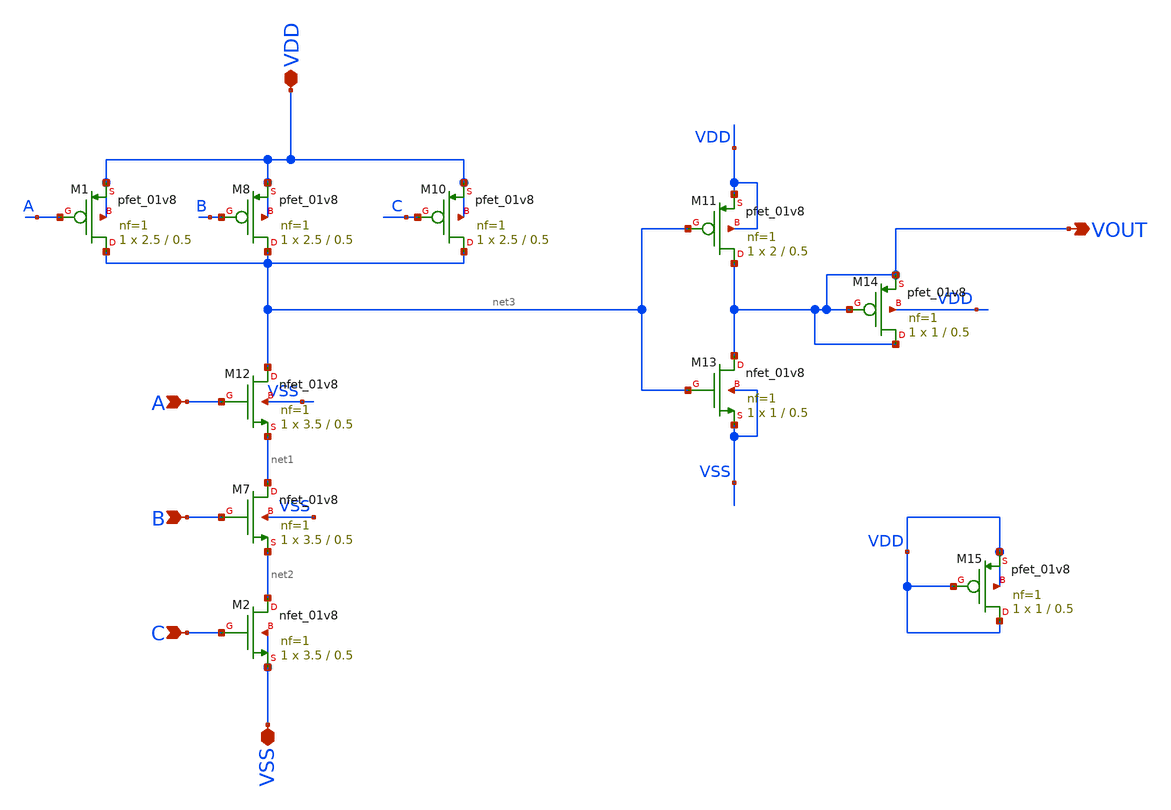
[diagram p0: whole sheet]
** sch_path: Xschem/TOP/3_inp_AND.sch
**.subckt 3_inp_AND VSS VDD A B C VOUT
*.iopin VSS
*.iopin VDD
*.ipin A
*.ipin B
*.ipin C
*.opin VOUT
XM2 net2 C VSS VSS sky130_fd_pr__nfet_01v8 L=0.5 W=3.5 nf=1 ad='int((nf+1)/2) * W/nf * 0.29' as='int((nf+2)/2) * W/nf * 0.29'
+ pd='2*int((nf+1)/2) * (W/nf + 0.29)' ps='2*int((nf+2)/2) * (W/nf + 0.29)' nrd='0.29 / W' nrs='0.29 / W'
+ sa=0 sb=0 sd=0 mult=1 m=1
XM7 net1 B net2 VSS sky130_fd_pr__nfet_01v8 L=0.5 W=3.5 nf=1 ad='int((nf+1)/2) * W/nf * 0.29' as='int((nf+2)/2) * W/nf * 0.29'
+ pd='2*int((nf+1)/2) * (W/nf + 0.29)' ps='2*int((nf+2)/2) * (W/nf + 0.29)' nrd='0.29 / W' nrs='0.29 / W'
+ sa=0 sb=0 sd=0 mult=1 m=1
XM1 net3 A VDD VDD sky130_fd_pr__pfet_01v8 L=0.5 W=2.5 nf=1 ad='int((nf+1)/2) * W/nf * 0.29' as='int((nf+2)/2) * W/nf * 0.29'
+ pd='2*int((nf+1)/2) * (W/nf + 0.29)' ps='2*int((nf+2)/2) * (W/nf + 0.29)' nrd='0.29 / W' nrs='0.29 / W'
+ sa=0 sb=0 sd=0 mult=1 m=1
XM8 net3 B VDD VDD sky130_fd_pr__pfet_01v8 L=0.5 W=2.5 nf=1 ad='int((nf+1)/2) * W/nf * 0.29' as='int((nf+2)/2) * W/nf * 0.29'
+ pd='2*int((nf+1)/2) * (W/nf + 0.29)' ps='2*int((nf+2)/2) * (W/nf + 0.29)' nrd='0.29 / W' nrs='0.29 / W'
+ sa=0 sb=0 sd=0 mult=1 m=1
XM10 net3 C VDD VDD sky130_fd_pr__pfet_01v8 L=0.5 W=2.5 nf=1 ad='int((nf+1)/2) * W/nf * 0.29' as='int((nf+2)/2) * W/nf * 0.29'
+ pd='2*int((nf+1)/2) * (W/nf + 0.29)' ps='2*int((nf+2)/2) * (W/nf + 0.29)' nrd='0.29 / W' nrs='0.29 / W'
+ sa=0 sb=0 sd=0 mult=1 m=1
XM11 VOUT net3 VDD VDD sky130_fd_pr__pfet_01v8 L=0.5 W=2 nf=1 ad='int((nf+1)/2) * W/nf * 0.29' as='int((nf+2)/2) * W/nf * 0.29'
+ pd='2*int((nf+1)/2) * (W/nf + 0.29)' ps='2*int((nf+2)/2) * (W/nf + 0.29)' nrd='0.29 / W' nrs='0.29 / W'
+ sa=0 sb=0 sd=0 mult=1 m=1
XM12 net3 A net1 VSS sky130_fd_pr__nfet_01v8 L=0.5 W=3.5 nf=1 ad='int((nf+1)/2) * W/nf * 0.29' as='int((nf+2)/2) * W/nf * 0.29'
+ pd='2*int((nf+1)/2) * (W/nf + 0.29)' ps='2*int((nf+2)/2) * (W/nf + 0.29)' nrd='0.29 / W' nrs='0.29 / W'
+ sa=0 sb=0 sd=0 mult=1 m=1
XM13 VOUT net3 VSS VSS sky130_fd_pr__nfet_01v8 L=0.5 W=1 nf=1 ad='int((nf+1)/2) * W/nf * 0.29' as='int((nf+2)/2) * W/nf * 0.29'
+ pd='2*int((nf+1)/2) * (W/nf + 0.29)' ps='2*int((nf+2)/2) * (W/nf + 0.29)' nrd='0.29 / W' nrs='0.29 / W'
+ sa=0 sb=0 sd=0 mult=1 m=1
XM14 VOUT VOUT VOUT VDD sky130_fd_pr__pfet_01v8 L=0.5 W=1 nf=1 ad='int((nf+1)/2) * W/nf * 0.29' as='int((nf+2)/2) * W/nf * 0.29'
+ pd='2*int((nf+1)/2) * (W/nf + 0.29)' ps='2*int((nf+2)/2) * (W/nf + 0.29)' nrd='0.29 / W' nrs='0.29 / W'
+ sa=0 sb=0 sd=0 mult=1 m=1
XM15 VDD VDD VDD VDD sky130_fd_pr__pfet_01v8 L=0.5 W=1 nf=1 ad='int((nf+1)/2) * W/nf * 0.29' as='int((nf+2)/2) * W/nf * 0.29'
+ pd='2*int((nf+1)/2) * (W/nf + 0.29)' ps='2*int((nf+2)/2) * (W/nf + 0.29)' nrd='0.29 / W' nrs='0.29 / W'
+ sa=0 sb=0 sd=0 mult=1 m=1
**.ends
.end
